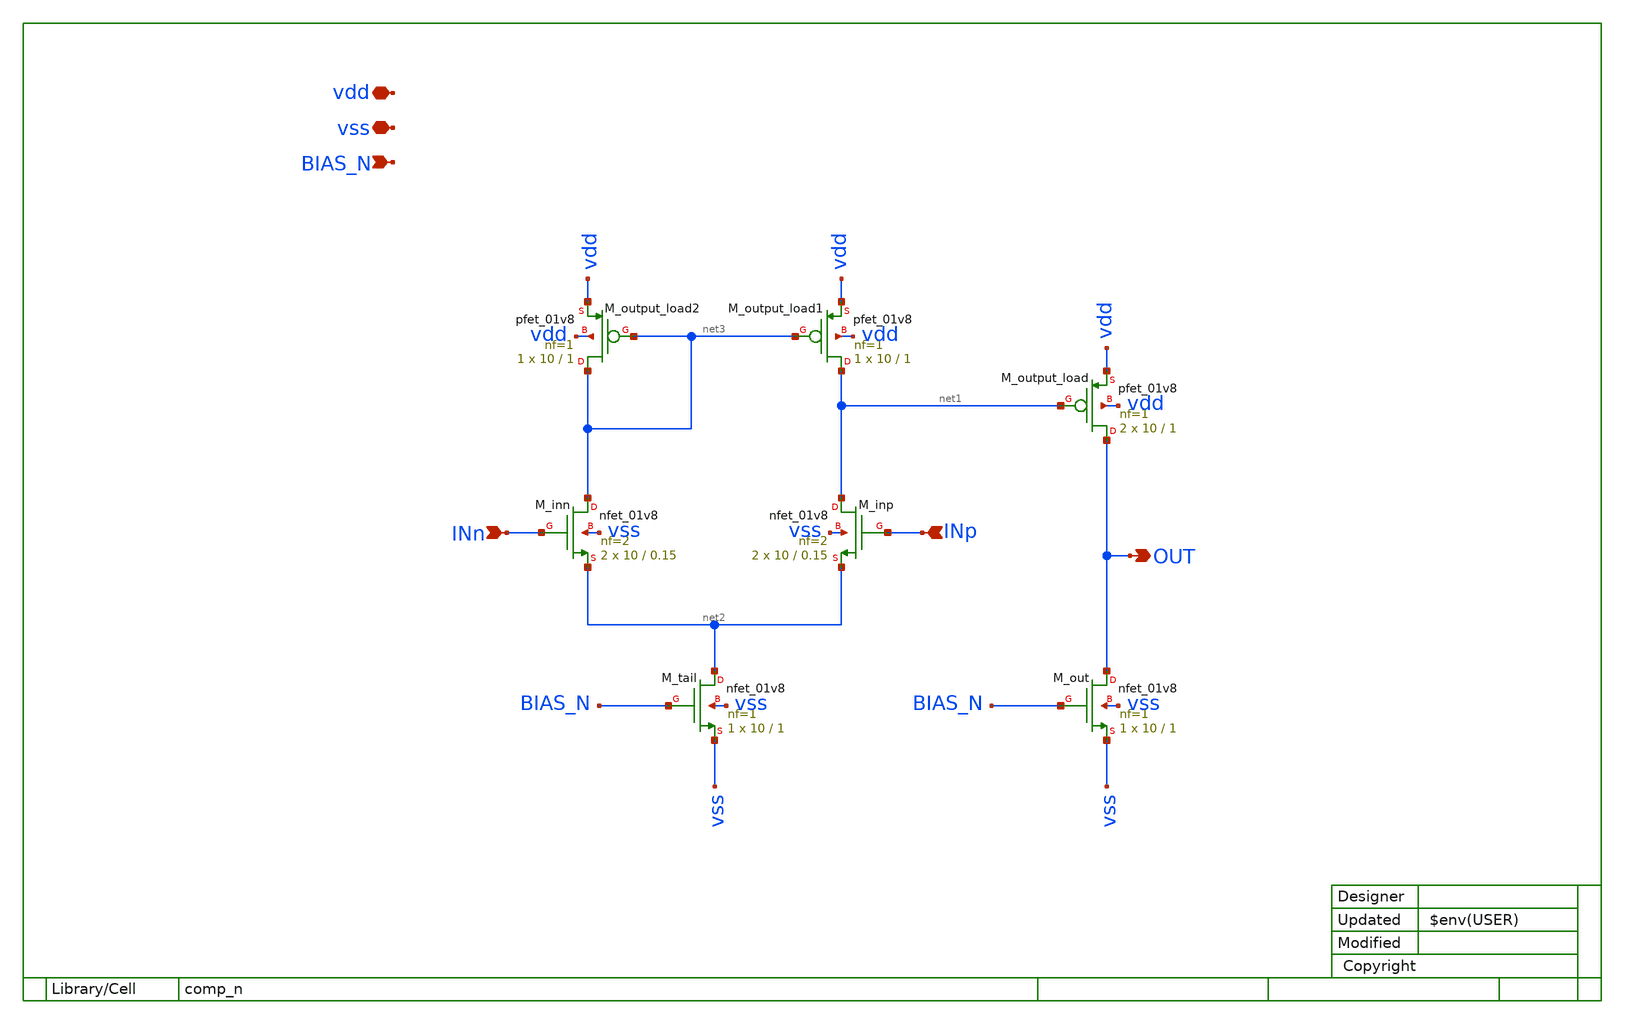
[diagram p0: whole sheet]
** sch_path: xsch/ip/comp_n.sch
**.subckt comp_n vdd OUT vss BIAS_N INn INp
*.iopin vdd
*.opin OUT
*.iopin vss
*.ipin BIAS_N
*.ipin INn
*.ipin INp
XM_tail net2 BIAS_N vss vss sky130_fd_pr__nfet_01v8 L=1 W=10 nf=1 ad='int((1 + 1)/2) * 10 / 1 * 0.29'
+ as='int((1 + 2)/2) * 10 / 1 * 0.29' pd='2*int((1 + 1)/2) * (10 / 1 + 0.29)' ps='2*int((1 + 2)/2) * (10 / 1 + 0.29)'
+ nrd='0.29 / 10 ' nrs='0.29 / 10 ' sa=0 sb=0 sd=0 mult=1 m=1
XM_out OUT BIAS_N vss vss sky130_fd_pr__nfet_01v8 L=1 W=10 nf=1 ad='int((1 + 1)/2) * 10 / 1 * 0.29' as='int((1 + 2)/2) * 10 / 1 * 0.29'
+ pd='2*int((1 + 1)/2) * (10 / 1 + 0.29)' ps='2*int((1 + 2)/2) * (10 / 1 + 0.29)' nrd='0.29 / 10 ' nrs='0.29 / 10 '
+ sa=0 sb=0 sd=0 mult=1 m=1
XM_output_load OUT net1 vdd vdd sky130_fd_pr__pfet_01v8 L=1 W=10 nf=1 ad='int((nf+1)/2) * W/nf * 0.29'
+ as='int((nf+2)/2) * W/nf * 0.29' pd='2*int((nf+1)/2) * (W/nf + 0.29)' ps='2*int((nf+2)/2) * (W/nf + 0.29)'
+ nrd='0.29 / W' nrs='0.29 / W' sa=0 sb=0 sd=0 mult=2 m=2
XM_inn net3 INn net2 vss sky130_fd_pr__nfet_01v8 L=0.15 W=10 nf=2 ad='int((2 + 1)/2) * 10 / 2 * 0.29'
+ as='int((2 + 2)/2) * 10 / 2 * 0.29' pd='2*int((2 + 1)/2) * (10 / 2 + 0.29)' ps='2*int((2 + 2)/2) * (10 / 2 + 0.29)'
+ nrd='0.29 / 10 ' nrs='0.29 / 10 ' sa=0 sb=0 sd=0 mult=2 m=2
XM_inp net1 INp net2 vss sky130_fd_pr__nfet_01v8 L=0.15 W=10 nf=2 ad='int((2 + 1)/2) * 10 / 2 * 0.29'
+ as='int((2 + 2)/2) * 10 / 2 * 0.29' pd='2*int((2 + 1)/2) * (10 / 2 + 0.29)' ps='2*int((2 + 2)/2) * (10 / 2 + 0.29)'
+ nrd='0.29 / 10 ' nrs='0.29 / 10 ' sa=0 sb=0 sd=0 mult=2 m=2
XM_output_load1 net1 net3 vdd vdd sky130_fd_pr__pfet_01v8 L=1 W=10 nf=1 ad='int((nf+1)/2) * W/nf * 0.29'
+ as='int((nf+2)/2) * W/nf * 0.29' pd='2*int((nf+1)/2) * (W/nf + 0.29)' ps='2*int((nf+2)/2) * (W/nf + 0.29)'
+ nrd='0.29 / W' nrs='0.29 / W' sa=0 sb=0 sd=0 mult=1 m=1
XM_output_load2 net3 net3 vdd vdd sky130_fd_pr__pfet_01v8 L=1 W=10 nf=1 ad='int((nf+1)/2) * W/nf * 0.29'
+ as='int((nf+2)/2) * W/nf * 0.29' pd='2*int((nf+1)/2) * (W/nf + 0.29)' ps='2*int((nf+2)/2) * (W/nf + 0.29)'
+ nrd='0.29 / W' nrs='0.29 / W' sa=0 sb=0 sd=0 mult=1 m=1
**.ends
.end
